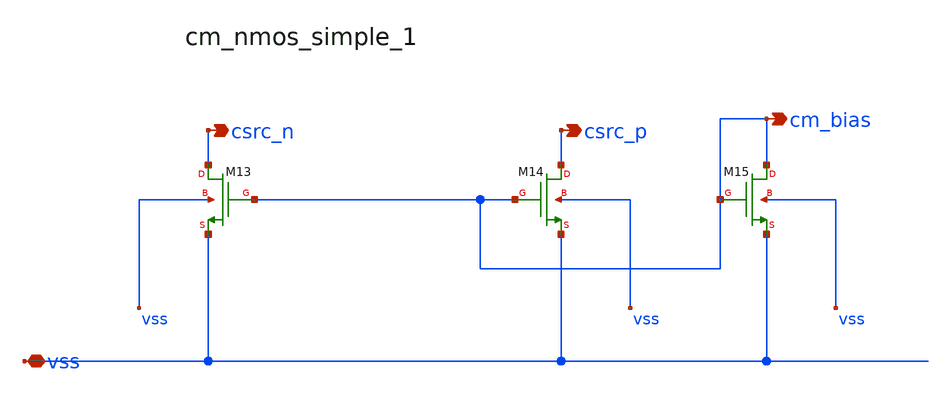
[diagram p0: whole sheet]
** sch_path: analog-db/raw/amp_027_fan_rrl_ota/hier/blocks/cm_nmos_simple_1.sch
**.subckt cm_nmos_simple_1 vss csrc_n csrc_p cm_bias
*.iopin vss
*.opin csrc_n
*.opin csrc_p
*.opin cm_bias
XM13 csrc_n cm_bias vss vss sg13_lv_nmos w=x_dut_xm13_w l=x_dut_xm13_l ng=1 m=x_dut_xm13_m
XM14 csrc_p cm_bias vss vss sg13_lv_nmos w=x_dut_xm14_w l=x_dut_xm14_l ng=1 m=x_dut_xm14_m
XM15 cm_bias cm_bias vss vss sg13_lv_nmos w=x_dut_xm15_w l=x_dut_xm15_l ng=1 m=x_dut_xm15_m
**.ends
.end
